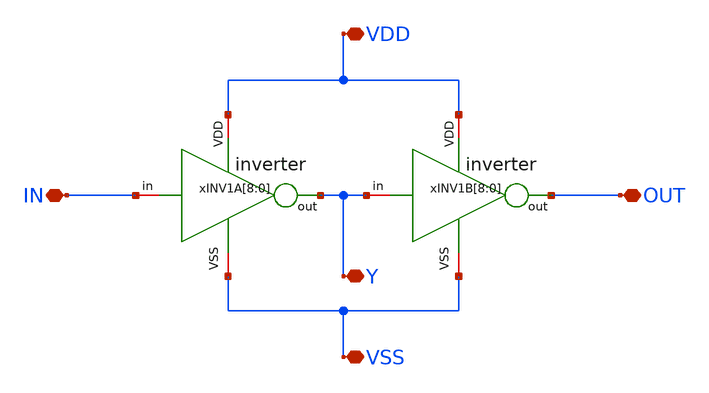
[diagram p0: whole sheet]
** sch_path: designs/sar_adc/digital/buffer_x1/xschem/buffer_SW1.sch
**.subckt buffer_SW1 OUT VSS VDD IN Y
*.iopin OUT
*.iopin VSS
*.iopin VDD
*.iopin IN
*.iopin Y
xINV1A[8] VDD IN Y VSS inverter
xINV1A[7] VDD IN Y VSS inverter
xINV1A[6] VDD IN Y VSS inverter
xINV1A[5] VDD IN Y VSS inverter
xINV1A[4] VDD IN Y VSS inverter
xINV1A[3] VDD IN Y VSS inverter
xINV1A[2] VDD IN Y VSS inverter
xINV1A[1] VDD IN Y VSS inverter
xINV1A[0] VDD IN Y VSS inverter
xINV1B[8] VDD Y OUT VSS inverter
xINV1B[7] VDD Y OUT VSS inverter
xINV1B[6] VDD Y OUT VSS inverter
xINV1B[5] VDD Y OUT VSS inverter
xINV1B[4] VDD Y OUT VSS inverter
xINV1B[3] VDD Y OUT VSS inverter
xINV1B[2] VDD Y OUT VSS inverter
xINV1B[1] VDD Y OUT VSS inverter
xINV1B[0] VDD Y OUT VSS inverter
**.ends

* expanding   symbol:  designs/sar_adc/digital/buffer_inv_x1/xschem/inverter.sym # of pins=6
** sym_path: designs/sar_adc/digital/buffer_inv_x1/xschem/inverter.sym
** sch_path: designs/sar_adc/digital/buffer_inv_x1/xschem/inverter.sch
.subckt inverter VDD in out VSS
*.opin out
*.iopin in
*.iopin VDD
*.iopin VSS
XM1 out in VSS VSS nfet_03v3 L=0.56u W=0.25u nf=1 ad='int((nf+1)/2) * W/nf * 0.18u' as='int((nf+2)/2) * W/nf * 0.18u'
+ pd='2*int((nf+1)/2) * (W/nf + 0.18u)' ps='2*int((nf+2)/2) * (W/nf + 0.18u)' nrd='0.18u / W' nrs='0.18u / W'
+ sa=0 sb=0 sd=0 m=2
XM2 out in VDD VDD pfet_03v3 L=0.56u W=0.25u nf=1 ad='int((nf+1)/2) * W/nf * 0.18u' as='int((nf+2)/2) * W/nf * 0.18u'
+ pd='2*int((nf+1)/2) * (W/nf + 0.18u)' ps='2*int((nf+2)/2) * (W/nf + 0.18u)' nrd='0.18u / W' nrs='0.18u / W'
+ sa=0 sb=0 sd=0 m=4
.ends

.end
